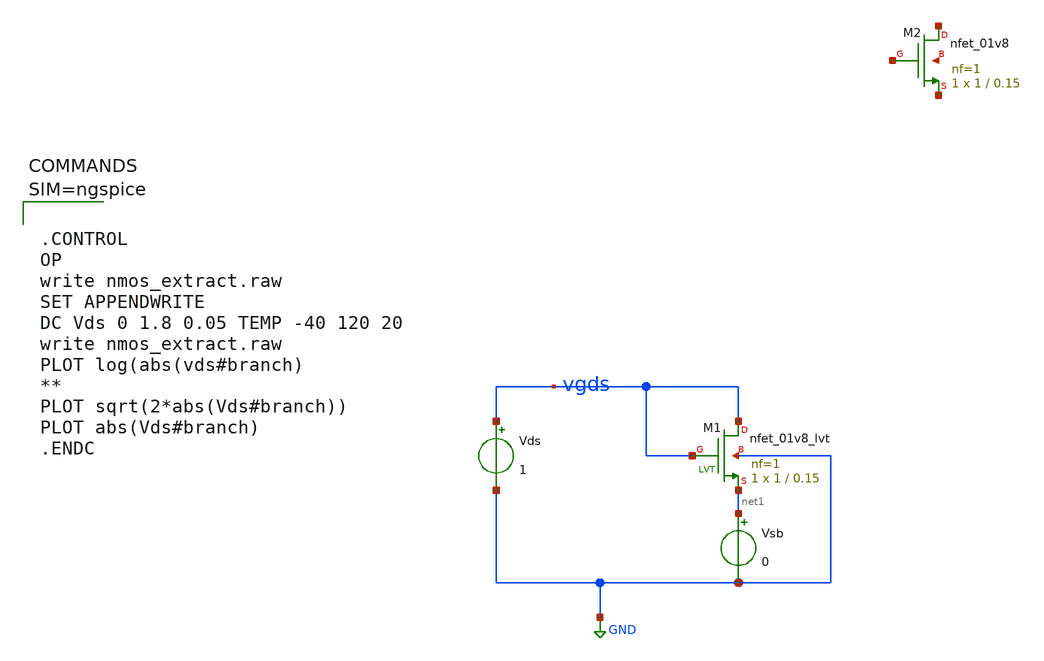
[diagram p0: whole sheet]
** sch_path: xschem/nmos_extract.sch
**.subckt nmos_extract
XM1 vgds vgds net1 GND sky130_fd_pr__nfet_01v8_lvt L=0.15 W=1 nf=1 ad='int((1 + 1)/2) * 1 / 1 * 0.29'
+ as='int((1 + 2)/2) * 1 / 1 * 0.29' pd='2*int((1 + 1)/2) * (1 / 1 + 0.29)' ps='2*int((1 + 2)/2) * (1 / 1 + 0.29)'
+ nrd='0.29 / 1 ' nrs='0.29 / 1 ' sa=0 sb=0 sd=0 mult=1 m=1
Vds vgds GND 1
Vsb net1 GND 0
XM2 net2 net3 net4 net5 sky130_fd_pr__nfet_01v8 L=0.15 W=1 nf=1 ad='int((1 + 1)/2) * 1 / 1 * 0.29' as='int((1 + 2)/2) * 1 / 1 * 0.29'
+ pd='2*int((1 + 1)/2) * (1 / 1 + 0.29)' ps='2*int((1 + 2)/2) * (1 / 1 + 0.29)' nrd='0.29 / 1 ' nrs='0.29 / 1 '
+ sa=0 sb=0 sd=0 mult=1 m=1
**** begin user architecture code



.CONTROL
OP
write nmos_extract.raw
SET APPENDWRITE
DC Vds 0 1.8 0.05 TEMP -40 120 20
write nmos_extract.raw
PLOT log(abs(vds#branch)
**
PLOT sqrt(2*abs(Vds#branch))
PLOT abs(Vds#branch)
.ENDC




** opencircuitdesign pdks install
.lib $::SKYWATER_MODELS/sky130.lib.spice tt

**** end user architecture code
**.ends
.GLOBAL GND
.end
